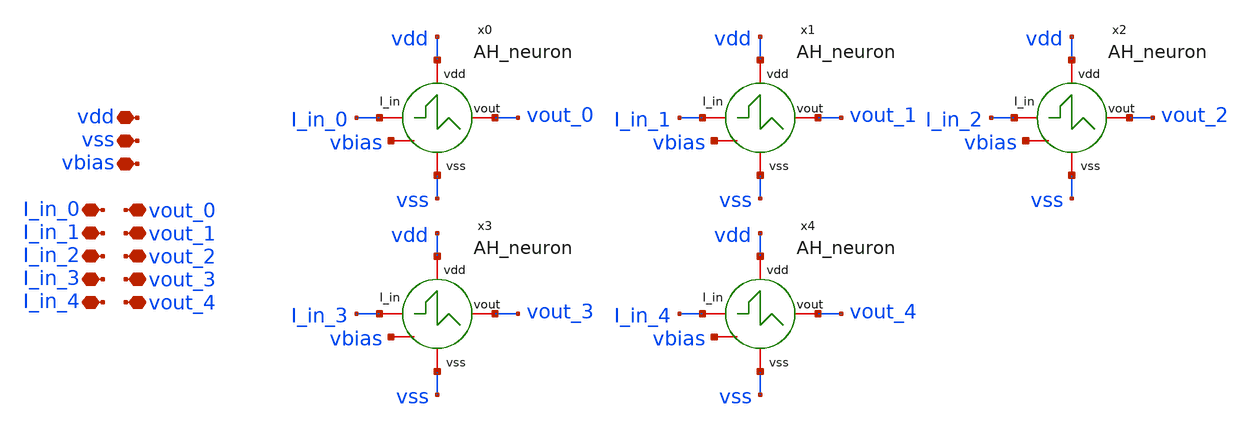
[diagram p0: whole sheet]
** sch_path: designs/libs/core_AH_neuron_arr/AH_neuron_arr.sch
**.subckt AH_neuron_arr vdd vss I_in_0 vout_0 I_in_1 vout_1 I_in_2 vout_2 I_in_3 vout_3 I_in_4
*+ vout_4 vbias
*.iopin vdd
*.iopin vss
*.iopin I_in_0
*.iopin vout_0
*.iopin I_in_1
*.iopin vout_1
*.iopin I_in_2
*.iopin vout_2
*.iopin I_in_3
*.iopin vout_3
*.iopin I_in_4
*.iopin vout_4
*.iopin vbias
x3 vdd I_in_3 vout_3 vss vbias AH_neuron
x0 vdd I_in_0 vout_0 vss vbias AH_neuron
x1 vdd I_in_1 vout_1 vss vbias AH_neuron
x4 vdd I_in_4 vout_4 vss vbias AH_neuron
x2 vdd I_in_2 vout_2 vss vbias AH_neuron
**.ends
.end
